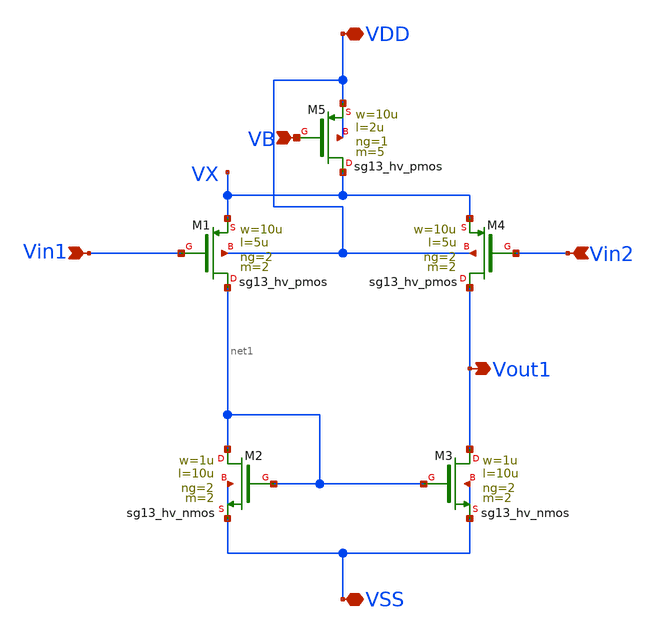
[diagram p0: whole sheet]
** sch_path: dependencies/PMU/PMU-main/schematic/xschem/Stage1.sch
**.subckt Stage1 VDD VB Vin1 Vin2 VSS Vout1
*.iopin VDD
*.ipin VB
*.ipin Vin1
*.ipin Vin2
*.iopin VSS
*.opin Vout1
XM1 net1 Vin1 VX VDD sg13_hv_pmos w=10u l=5u ng=2 m=2 mm_ok=1
XM2 net1 net1 VSS VSS sg13_hv_nmos w=1u l=10u ng=2 m=2 mm_ok=1
XM3 Vout1 net1 VSS VSS sg13_hv_nmos w=1u l=10u ng=2 m=2 mm_ok=1
XM4 Vout1 Vin2 VX VDD sg13_hv_pmos w=10u l=5u ng=2 m=2 mm_ok=1
XM5 VX VB VDD VDD sg13_hv_pmos w=10u l=2u ng=1 m=5 mm_ok=1
**.ends
.end
